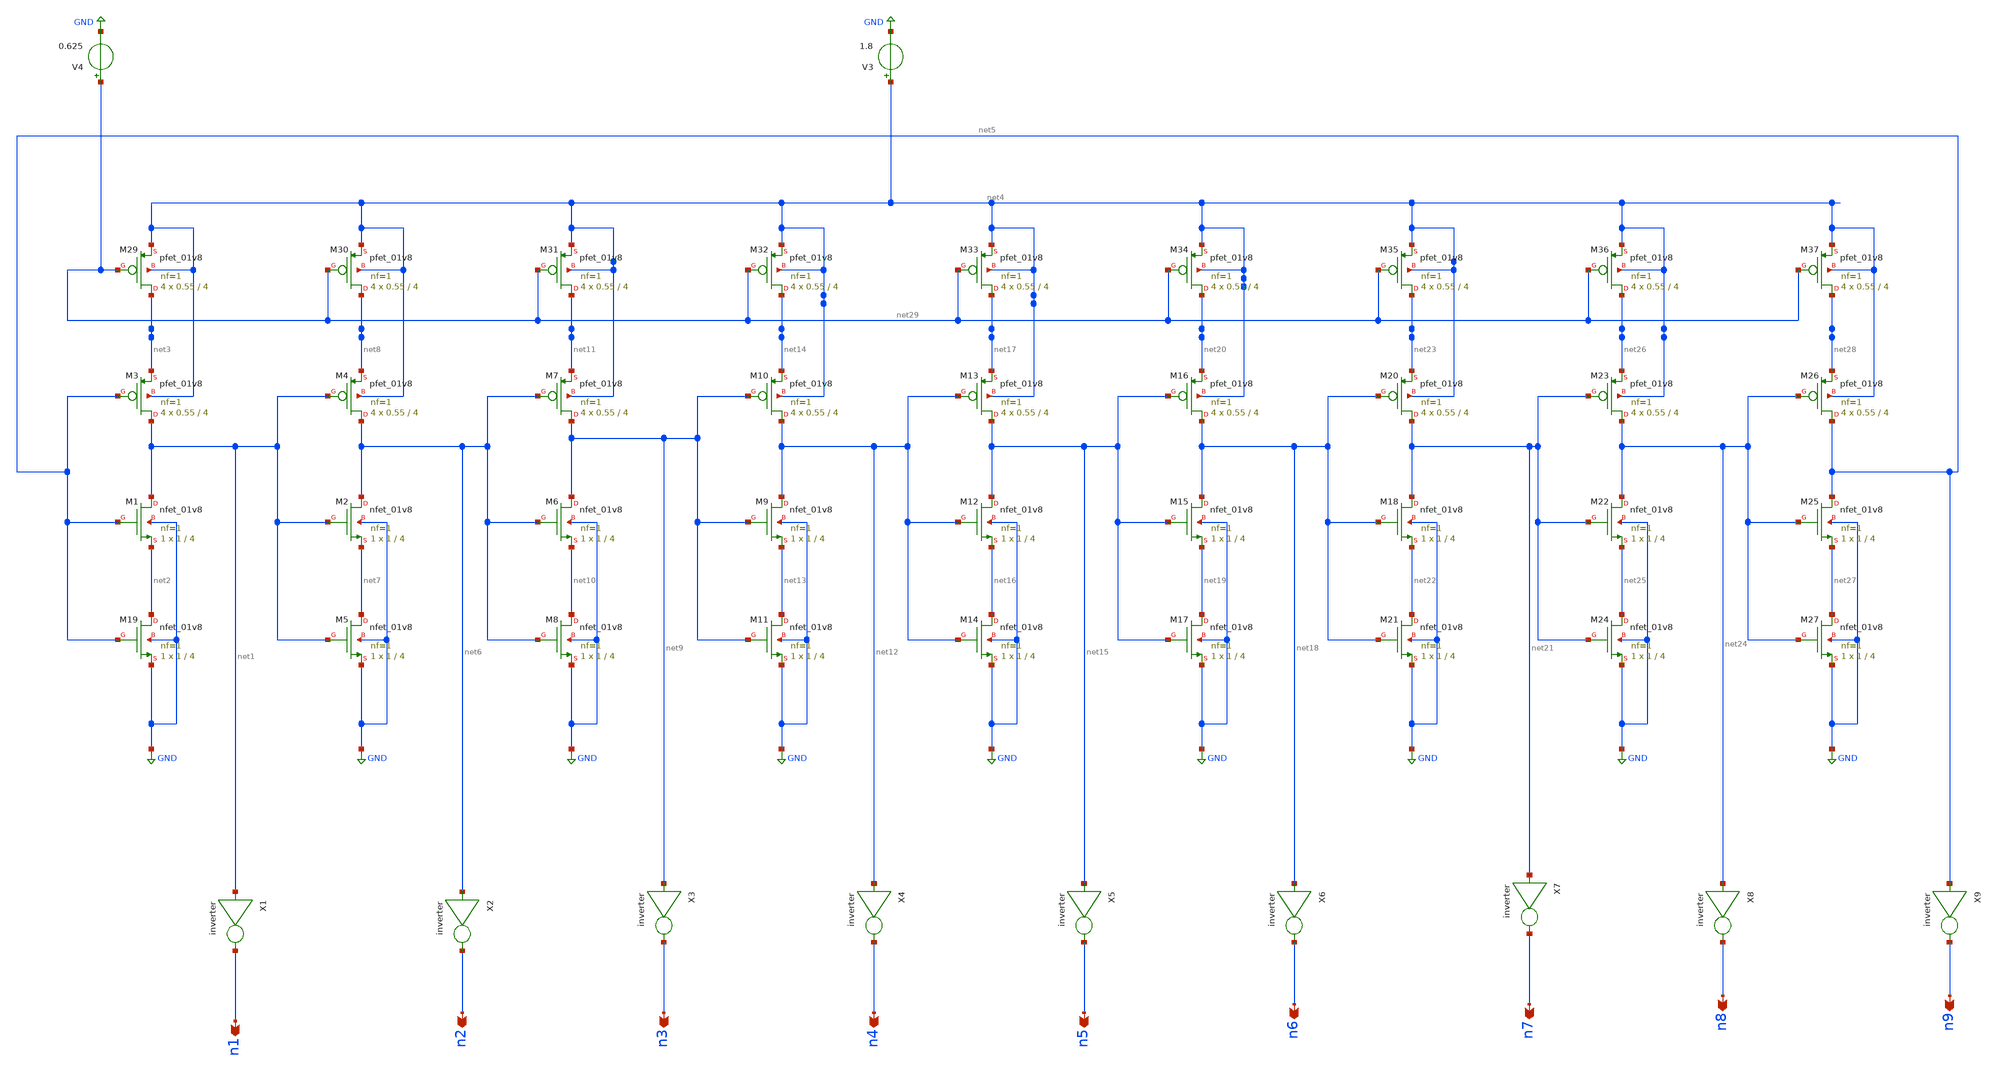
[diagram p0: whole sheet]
** sch_path: ringoscillator.sch
**.subckt ringoscillator n1 n2 n3 n4 n5 n6 n8 n9 n7
*.opin n1
*.opin n2
*.opin n3
*.opin n4
*.opin n5
*.opin n6
*.opin n8
*.opin n9
*.opin n7
XM1 net1 net5 net2 GND sky130_fd_pr__nfet_01v8 L=4 W=1 nf=1 ad='int((nf+1)/2) * W/nf * 0.29' as='int((nf+2)/2) * W/nf * 0.29'
+ pd='2*int((nf+1)/2) * (W/nf + 0.29)' ps='2*int((nf+2)/2) * (W/nf + 0.29)' nrd='0.29 / W' nrs='0.29 / W'
+ sa=0 sb=0 sd=0 mult=1 m=1
XM3 net1 net5 net3 net4 sky130_fd_pr__pfet_01v8 L=4 W=0.55 nf=1 ad='int((nf+1)/2) * W/nf * 0.29' as='int((nf+2)/2) * W/nf * 0.29'
+ pd='2*int((nf+1)/2) * (W/nf + 0.29)' ps='2*int((nf+2)/2) * (W/nf + 0.29)' nrd='0.29 / W' nrs='0.29 / W'
+ sa=0 sb=0 sd=0 mult=4 m=4
XM19 net2 net5 GND GND sky130_fd_pr__nfet_01v8 L=4 W=1 nf=1 ad='int((nf+1)/2) * W/nf * 0.29' as='int((nf+2)/2) * W/nf * 0.29'
+ pd='2*int((nf+1)/2) * (W/nf + 0.29)' ps='2*int((nf+2)/2) * (W/nf + 0.29)' nrd='0.29 / W' nrs='0.29 / W'
+ sa=0 sb=0 sd=0 mult=1 m=1
XM2 net6 net1 net7 GND sky130_fd_pr__nfet_01v8 L=4 W=1 nf=1 ad='int((nf+1)/2) * W/nf * 0.29' as='int((nf+2)/2) * W/nf * 0.29'
+ pd='2*int((nf+1)/2) * (W/nf + 0.29)' ps='2*int((nf+2)/2) * (W/nf + 0.29)' nrd='0.29 / W' nrs='0.29 / W'
+ sa=0 sb=0 sd=0 mult=1 m=1
XM4 net6 net1 net8 net4 sky130_fd_pr__pfet_01v8 L=4 W=0.55 nf=1 ad='int((nf+1)/2) * W/nf * 0.29' as='int((nf+2)/2) * W/nf * 0.29'
+ pd='2*int((nf+1)/2) * (W/nf + 0.29)' ps='2*int((nf+2)/2) * (W/nf + 0.29)' nrd='0.29 / W' nrs='0.29 / W'
+ sa=0 sb=0 sd=0 mult=4 m=4
XM5 net7 net1 GND GND sky130_fd_pr__nfet_01v8 L=4 W=1 nf=1 ad='int((nf+1)/2) * W/nf * 0.29' as='int((nf+2)/2) * W/nf * 0.29'
+ pd='2*int((nf+1)/2) * (W/nf + 0.29)' ps='2*int((nf+2)/2) * (W/nf + 0.29)' nrd='0.29 / W' nrs='0.29 / W'
+ sa=0 sb=0 sd=0 mult=1 m=1
XM6 net9 net6 net10 GND sky130_fd_pr__nfet_01v8 L=4 W=1 nf=1 ad='int((nf+1)/2) * W/nf * 0.29' as='int((nf+2)/2) * W/nf * 0.29'
+ pd='2*int((nf+1)/2) * (W/nf + 0.29)' ps='2*int((nf+2)/2) * (W/nf + 0.29)' nrd='0.29 / W' nrs='0.29 / W'
+ sa=0 sb=0 sd=0 mult=1 m=1
XM7 net9 net6 net11 net4 sky130_fd_pr__pfet_01v8 L=4 W=0.55 nf=1 ad='int((nf+1)/2) * W/nf * 0.29' as='int((nf+2)/2) * W/nf * 0.29'
+ pd='2*int((nf+1)/2) * (W/nf + 0.29)' ps='2*int((nf+2)/2) * (W/nf + 0.29)' nrd='0.29 / W' nrs='0.29 / W'
+ sa=0 sb=0 sd=0 mult=4 m=4
XM8 net10 net6 GND GND sky130_fd_pr__nfet_01v8 L=4 W=1 nf=1 ad='int((nf+1)/2) * W/nf * 0.29' as='int((nf+2)/2) * W/nf * 0.29'
+ pd='2*int((nf+1)/2) * (W/nf + 0.29)' ps='2*int((nf+2)/2) * (W/nf + 0.29)' nrd='0.29 / W' nrs='0.29 / W'
+ sa=0 sb=0 sd=0 mult=1 m=1
XM9 net12 net9 net13 GND sky130_fd_pr__nfet_01v8 L=4 W=1 nf=1 ad='int((nf+1)/2) * W/nf * 0.29' as='int((nf+2)/2) * W/nf * 0.29'
+ pd='2*int((nf+1)/2) * (W/nf + 0.29)' ps='2*int((nf+2)/2) * (W/nf + 0.29)' nrd='0.29 / W' nrs='0.29 / W'
+ sa=0 sb=0 sd=0 mult=1 m=1
XM10 net12 net9 net14 net4 sky130_fd_pr__pfet_01v8 L=4 W=0.55 nf=1 ad='int((nf+1)/2) * W/nf * 0.29' as='int((nf+2)/2) * W/nf * 0.29'
+ pd='2*int((nf+1)/2) * (W/nf + 0.29)' ps='2*int((nf+2)/2) * (W/nf + 0.29)' nrd='0.29 / W' nrs='0.29 / W'
+ sa=0 sb=0 sd=0 mult=4 m=4
XM11 net13 net9 GND GND sky130_fd_pr__nfet_01v8 L=4 W=1 nf=1 ad='int((nf+1)/2) * W/nf * 0.29' as='int((nf+2)/2) * W/nf * 0.29'
+ pd='2*int((nf+1)/2) * (W/nf + 0.29)' ps='2*int((nf+2)/2) * (W/nf + 0.29)' nrd='0.29 / W' nrs='0.29 / W'
+ sa=0 sb=0 sd=0 mult=1 m=1
XM12 net15 net12 net16 GND sky130_fd_pr__nfet_01v8 L=4 W=1 nf=1 ad='int((nf+1)/2) * W/nf * 0.29' as='int((nf+2)/2) * W/nf * 0.29'
+ pd='2*int((nf+1)/2) * (W/nf + 0.29)' ps='2*int((nf+2)/2) * (W/nf + 0.29)' nrd='0.29 / W' nrs='0.29 / W'
+ sa=0 sb=0 sd=0 mult=1 m=1
XM13 net15 net12 net17 net4 sky130_fd_pr__pfet_01v8 L=4 W=0.55 nf=1 ad='int((nf+1)/2) * W/nf * 0.29'
+ as='int((nf+2)/2) * W/nf * 0.29' pd='2*int((nf+1)/2) * (W/nf + 0.29)' ps='2*int((nf+2)/2) * (W/nf + 0.29)'
+ nrd='0.29 / W' nrs='0.29 / W' sa=0 sb=0 sd=0 mult=4 m=4
XM14 net16 net12 GND GND sky130_fd_pr__nfet_01v8 L=4 W=1 nf=1 ad='int((nf+1)/2) * W/nf * 0.29' as='int((nf+2)/2) * W/nf * 0.29'
+ pd='2*int((nf+1)/2) * (W/nf + 0.29)' ps='2*int((nf+2)/2) * (W/nf + 0.29)' nrd='0.29 / W' nrs='0.29 / W'
+ sa=0 sb=0 sd=0 mult=1 m=1
XM15 net18 net15 net19 GND sky130_fd_pr__nfet_01v8 L=4 W=1 nf=1 ad='int((nf+1)/2) * W/nf * 0.29' as='int((nf+2)/2) * W/nf * 0.29'
+ pd='2*int((nf+1)/2) * (W/nf + 0.29)' ps='2*int((nf+2)/2) * (W/nf + 0.29)' nrd='0.29 / W' nrs='0.29 / W'
+ sa=0 sb=0 sd=0 mult=1 m=1
XM16 net18 net15 net20 net4 sky130_fd_pr__pfet_01v8 L=4 W=0.55 nf=1 ad='int((nf+1)/2) * W/nf * 0.29'
+ as='int((nf+2)/2) * W/nf * 0.29' pd='2*int((nf+1)/2) * (W/nf + 0.29)' ps='2*int((nf+2)/2) * (W/nf + 0.29)'
+ nrd='0.29 / W' nrs='0.29 / W' sa=0 sb=0 sd=0 mult=4 m=4
XM17 net19 net15 GND GND sky130_fd_pr__nfet_01v8 L=4 W=1 nf=1 ad='int((nf+1)/2) * W/nf * 0.29' as='int((nf+2)/2) * W/nf * 0.29'
+ pd='2*int((nf+1)/2) * (W/nf + 0.29)' ps='2*int((nf+2)/2) * (W/nf + 0.29)' nrd='0.29 / W' nrs='0.29 / W'
+ sa=0 sb=0 sd=0 mult=1 m=1
XM18 net21 net18 net22 GND sky130_fd_pr__nfet_01v8 L=4 W=1 nf=1 ad='int((nf+1)/2) * W/nf * 0.29' as='int((nf+2)/2) * W/nf * 0.29'
+ pd='2*int((nf+1)/2) * (W/nf + 0.29)' ps='2*int((nf+2)/2) * (W/nf + 0.29)' nrd='0.29 / W' nrs='0.29 / W'
+ sa=0 sb=0 sd=0 mult=1 m=1
XM20 net21 net18 net23 net4 sky130_fd_pr__pfet_01v8 L=4 W=0.55 nf=1 ad='int((nf+1)/2) * W/nf * 0.29'
+ as='int((nf+2)/2) * W/nf * 0.29' pd='2*int((nf+1)/2) * (W/nf + 0.29)' ps='2*int((nf+2)/2) * (W/nf + 0.29)'
+ nrd='0.29 / W' nrs='0.29 / W' sa=0 sb=0 sd=0 mult=4 m=4
XM21 net22 net18 GND GND sky130_fd_pr__nfet_01v8 L=4 W=1 nf=1 ad='int((nf+1)/2) * W/nf * 0.29' as='int((nf+2)/2) * W/nf * 0.29'
+ pd='2*int((nf+1)/2) * (W/nf + 0.29)' ps='2*int((nf+2)/2) * (W/nf + 0.29)' nrd='0.29 / W' nrs='0.29 / W'
+ sa=0 sb=0 sd=0 mult=1 m=1
XM22 net24 net21 net25 GND sky130_fd_pr__nfet_01v8 L=4 W=1 nf=1 ad='int((nf+1)/2) * W/nf * 0.29' as='int((nf+2)/2) * W/nf * 0.29'
+ pd='2*int((nf+1)/2) * (W/nf + 0.29)' ps='2*int((nf+2)/2) * (W/nf + 0.29)' nrd='0.29 / W' nrs='0.29 / W'
+ sa=0 sb=0 sd=0 mult=1 m=1
XM23 net24 net21 net26 net4 sky130_fd_pr__pfet_01v8 L=4 W=0.55 nf=1 ad='int((nf+1)/2) * W/nf * 0.29'
+ as='int((nf+2)/2) * W/nf * 0.29' pd='2*int((nf+1)/2) * (W/nf + 0.29)' ps='2*int((nf+2)/2) * (W/nf + 0.29)'
+ nrd='0.29 / W' nrs='0.29 / W' sa=0 sb=0 sd=0 mult=4 m=4
XM24 net25 net21 GND GND sky130_fd_pr__nfet_01v8 L=4 W=1 nf=1 ad='int((nf+1)/2) * W/nf * 0.29' as='int((nf+2)/2) * W/nf * 0.29'
+ pd='2*int((nf+1)/2) * (W/nf + 0.29)' ps='2*int((nf+2)/2) * (W/nf + 0.29)' nrd='0.29 / W' nrs='0.29 / W'
+ sa=0 sb=0 sd=0 mult=1 m=1
XM25 net5 net24 net27 GND sky130_fd_pr__nfet_01v8 L=4 W=1 nf=1 ad='int((nf+1)/2) * W/nf * 0.29' as='int((nf+2)/2) * W/nf * 0.29'
+ pd='2*int((nf+1)/2) * (W/nf + 0.29)' ps='2*int((nf+2)/2) * (W/nf + 0.29)' nrd='0.29 / W' nrs='0.29 / W'
+ sa=0 sb=0 sd=0 mult=1 m=1
XM26 net5 net24 net28 net4 sky130_fd_pr__pfet_01v8 L=4 W=0.55 nf=1 ad='int((nf+1)/2) * W/nf * 0.29' as='int((nf+2)/2) * W/nf * 0.29'
+ pd='2*int((nf+1)/2) * (W/nf + 0.29)' ps='2*int((nf+2)/2) * (W/nf + 0.29)' nrd='0.29 / W' nrs='0.29 / W'
+ sa=0 sb=0 sd=0 mult=4 m=4
XM27 net27 net24 GND GND sky130_fd_pr__nfet_01v8 L=4 W=1 nf=1 ad='int((nf+1)/2) * W/nf * 0.29' as='int((nf+2)/2) * W/nf * 0.29'
+ pd='2*int((nf+1)/2) * (W/nf + 0.29)' ps='2*int((nf+2)/2) * (W/nf + 0.29)' nrd='0.29 / W' nrs='0.29 / W'
+ sa=0 sb=0 sd=0 mult=1 m=1
XM29 net3 net29 net4 net4 sky130_fd_pr__pfet_01v8 L=4 W=0.55 nf=1 ad='int((nf+1)/2) * W/nf * 0.29' as='int((nf+2)/2) * W/nf * 0.29'
+ pd='2*int((nf+1)/2) * (W/nf + 0.29)' ps='2*int((nf+2)/2) * (W/nf + 0.29)' nrd='0.29 / W' nrs='0.29 / W'
+ sa=0 sb=0 sd=0 mult=4 m=4
XM30 net8 net29 net4 net4 sky130_fd_pr__pfet_01v8 L=4 W=0.55 nf=1 ad='int((nf+1)/2) * W/nf * 0.29' as='int((nf+2)/2) * W/nf * 0.29'
+ pd='2*int((nf+1)/2) * (W/nf + 0.29)' ps='2*int((nf+2)/2) * (W/nf + 0.29)' nrd='0.29 / W' nrs='0.29 / W'
+ sa=0 sb=0 sd=0 mult=4 m=4
XM31 net11 net29 net4 net4 sky130_fd_pr__pfet_01v8 L=4 W=0.55 nf=1 ad='int((nf+1)/2) * W/nf * 0.29' as='int((nf+2)/2) * W/nf * 0.29'
+ pd='2*int((nf+1)/2) * (W/nf + 0.29)' ps='2*int((nf+2)/2) * (W/nf + 0.29)' nrd='0.29 / W' nrs='0.29 / W'
+ sa=0 sb=0 sd=0 mult=4 m=4
XM32 net14 net29 net4 net4 sky130_fd_pr__pfet_01v8 L=4 W=0.55 nf=1 ad='int((nf+1)/2) * W/nf * 0.29' as='int((nf+2)/2) * W/nf * 0.29'
+ pd='2*int((nf+1)/2) * (W/nf + 0.29)' ps='2*int((nf+2)/2) * (W/nf + 0.29)' nrd='0.29 / W' nrs='0.29 / W'
+ sa=0 sb=0 sd=0 mult=4 m=4
XM33 net17 net29 net4 net4 sky130_fd_pr__pfet_01v8 L=4 W=0.55 nf=1 ad='int((nf+1)/2) * W/nf * 0.29' as='int((nf+2)/2) * W/nf * 0.29'
+ pd='2*int((nf+1)/2) * (W/nf + 0.29)' ps='2*int((nf+2)/2) * (W/nf + 0.29)' nrd='0.29 / W' nrs='0.29 / W'
+ sa=0 sb=0 sd=0 mult=4 m=4
XM34 net20 net29 net4 net4 sky130_fd_pr__pfet_01v8 L=4 W=0.55 nf=1 ad='int((nf+1)/2) * W/nf * 0.29' as='int((nf+2)/2) * W/nf * 0.29'
+ pd='2*int((nf+1)/2) * (W/nf + 0.29)' ps='2*int((nf+2)/2) * (W/nf + 0.29)' nrd='0.29 / W' nrs='0.29 / W'
+ sa=0 sb=0 sd=0 mult=4 m=4
XM35 net23 net29 net4 net4 sky130_fd_pr__pfet_01v8 L=4 W=0.55 nf=1 ad='int((nf+1)/2) * W/nf * 0.29' as='int((nf+2)/2) * W/nf * 0.29'
+ pd='2*int((nf+1)/2) * (W/nf + 0.29)' ps='2*int((nf+2)/2) * (W/nf + 0.29)' nrd='0.29 / W' nrs='0.29 / W'
+ sa=0 sb=0 sd=0 mult=4 m=4
XM36 net26 net29 net4 net4 sky130_fd_pr__pfet_01v8 L=4 W=0.55 nf=1 ad='int((nf+1)/2) * W/nf * 0.29' as='int((nf+2)/2) * W/nf * 0.29'
+ pd='2*int((nf+1)/2) * (W/nf + 0.29)' ps='2*int((nf+2)/2) * (W/nf + 0.29)' nrd='0.29 / W' nrs='0.29 / W'
+ sa=0 sb=0 sd=0 mult=4 m=4
XM37 net28 net29 net4 net4 sky130_fd_pr__pfet_01v8 L=4 W=0.55 nf=1 ad='int((nf+1)/2) * W/nf * 0.29' as='int((nf+2)/2) * W/nf * 0.29'
+ pd='2*int((nf+1)/2) * (W/nf + 0.29)' ps='2*int((nf+2)/2) * (W/nf + 0.29)' nrd='0.29 / W' nrs='0.29 / W'
+ sa=0 sb=0 sd=0 mult=4 m=4
V3 net4 GND 1.8
V4 net29 GND 0.625
X1 net1 n1 inverter
X2 net6 n2 inverter
X3 net9 n3 inverter
X4 net12 n4 inverter
X5 net15 n5 inverter
X6 net18 n6 inverter
X7 net21 n7 inverter
X8 net24 n8 inverter
X9 net5 n9 inverter
**.ends

* expanding   symbol:  /home/cegrahul/Desktop/SSCS/inverter.sym # of pins=2
** sym_path: inverter.sym
** sch_path: inverter.sch
.subckt inverter vin vout
*.ipin vin
*.opin vout
XM2 vout vin net1 net1 sky130_fd_pr__pfet_01v8 L=0.15 W=1.68 nf=1 ad='int((nf+1)/2) * W/nf * 0.29' as='int((nf+2)/2) * W/nf * 0.29'
+ pd='2*int((nf+1)/2) * (W/nf + 0.29)' ps='2*int((nf+2)/2) * (W/nf + 0.29)' nrd='0.29 / W' nrs='0.29 / W'
+ sa=0 sb=0 sd=0 mult=1 m=1
XM3 vout vin GND GND sky130_fd_pr__nfet_01v8 L=0.15 W=0.36 nf=1 ad='int((nf+1)/2) * W/nf * 0.29' as='int((nf+2)/2) * W/nf * 0.29'
+ pd='2*int((nf+1)/2) * (W/nf + 0.29)' ps='2*int((nf+2)/2) * (W/nf + 0.29)' nrd='0.29 / W' nrs='0.29 / W'
+ sa=0 sb=0 sd=0 mult=1 m=1
V3 net1 GND 1.8
.ends

.GLOBAL GND
.end
